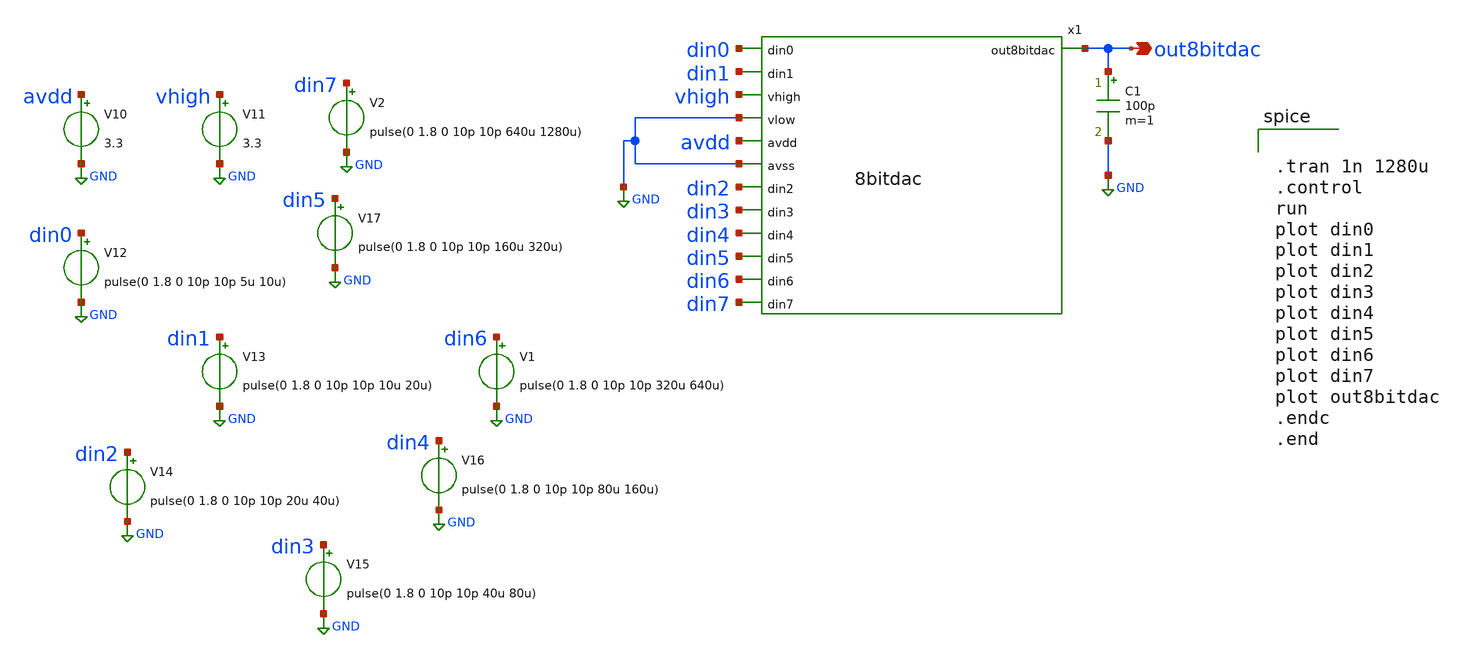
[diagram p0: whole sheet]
** sch_path: xschem/tb_8bitdac.sch
**.subckt tb_8bitdac out8bitdac
*.opin out8bitdac
x1 out8bitdac din0 din1 vhigh GND avdd GND din2 din3 din4 din5 din6 din7 8bitdac
V10 avdd GND 3.3
V11 vhigh GND 3.3
V12 din0 GND pulse(0 1.8 0 10p 10p 5u 10u)
V13 din1 GND pulse(0 1.8 0 10p 10p 10u 20u)
V14 din2 GND pulse(0 1.8 0 10p 10p 20u 40u)
V15 din3 GND pulse(0 1.8 0 10p 10p 40u 80u)
V16 din4 GND pulse(0 1.8 0 10p 10p 80u 160u)
V17 din5 GND pulse(0 1.8 0 10p 10p 160u 320u)
V1 din6 GND pulse(0 1.8 0 10p 10p 320u 640u)
V2 din7 GND pulse(0 1.8 0 10p 10p 640u 1280u)
C1 out8bitdac GND 100p m=1
**** begin user architecture code

** opencircuitdesign pdks install
.lib $::SKYWATER_MODELS/sky130.lib.spice tt




.tran 1n 1280u
.control
run
plot din0
plot din1
plot din2
plot din3
plot din4
plot din5
plot din6
plot din7
plot out8bitdac
.endc
.end

**** end user architecture code
**.ends
.GLOBAL GND
.end
